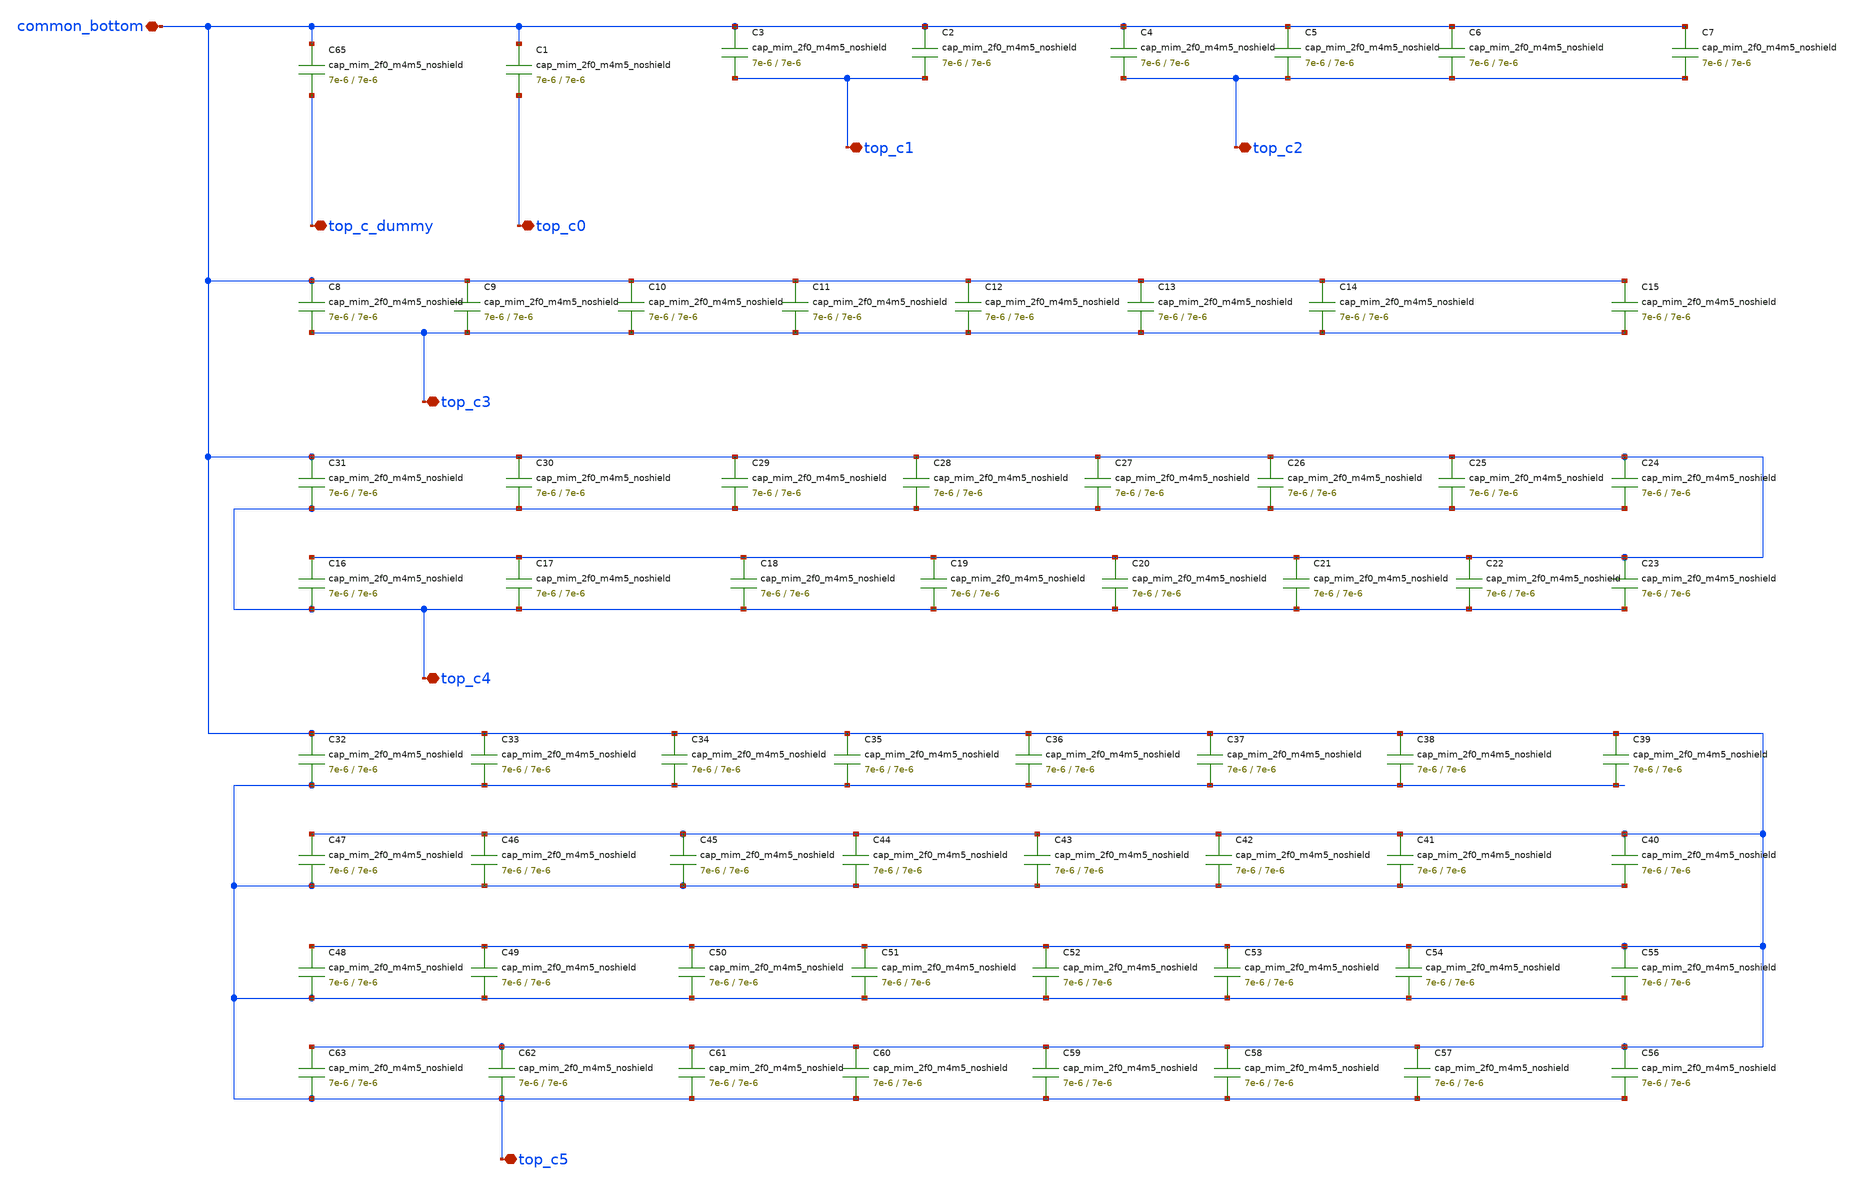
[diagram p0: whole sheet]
** sch_path: cdac/mim_cap_array_8x8/rev001/advanced_mimcap_array8x8_15step.sch
**.subckt advanced_mimcap_array8x8_15step common_bottom top_c1 top_c0 top_c_dummy top_c2 top_c4
*+ top_c5 top_c3
*.iopin common_bottom
*.iopin top_c1
*.iopin top_c0
*.iopin top_c_dummy
*.iopin top_c2
*.iopin top_c4
*.iopin top_c5
*.iopin top_c3
C65 common_bottom top_c_dummy cap_mim_2f0_m4m5_noshield W=7e-6 L=7e-6
C1 common_bottom top_c0 cap_mim_2f0_m4m5_noshield W=7e-6 L=7e-6
C2 common_bottom top_c1 cap_mim_2f0_m4m5_noshield W=7e-6 L=7e-6
C3 common_bottom top_c1 cap_mim_2f0_m4m5_noshield W=7e-6 L=7e-6
C4 common_bottom top_c2 cap_mim_2f0_m4m5_noshield W=7e-6 L=7e-6
C5 common_bottom top_c2 cap_mim_2f0_m4m5_noshield W=7e-6 L=7e-6
C6 common_bottom top_c2 cap_mim_2f0_m4m5_noshield W=7e-6 L=7e-6
C7 common_bottom top_c2 cap_mim_2f0_m4m5_noshield W=7e-6 L=7e-6
C8 common_bottom top_c3 cap_mim_2f0_m4m5_noshield W=7e-6 L=7e-6
C9 common_bottom top_c3 cap_mim_2f0_m4m5_noshield W=7e-6 L=7e-6
C10 common_bottom top_c3 cap_mim_2f0_m4m5_noshield W=7e-6 L=7e-6
C11 common_bottom top_c3 cap_mim_2f0_m4m5_noshield W=7e-6 L=7e-6
C12 common_bottom top_c3 cap_mim_2f0_m4m5_noshield W=7e-6 L=7e-6
C13 common_bottom top_c3 cap_mim_2f0_m4m5_noshield W=7e-6 L=7e-6
C14 common_bottom top_c3 cap_mim_2f0_m4m5_noshield W=7e-6 L=7e-6
C15 common_bottom top_c3 cap_mim_2f0_m4m5_noshield W=7e-6 L=7e-6
C16 common_bottom top_c4 cap_mim_2f0_m4m5_noshield W=7e-6 L=7e-6
C17 common_bottom top_c4 cap_mim_2f0_m4m5_noshield W=7e-6 L=7e-6
C18 common_bottom top_c4 cap_mim_2f0_m4m5_noshield W=7e-6 L=7e-6
C19 common_bottom top_c4 cap_mim_2f0_m4m5_noshield W=7e-6 L=7e-6
C20 common_bottom top_c4 cap_mim_2f0_m4m5_noshield W=7e-6 L=7e-6
C21 common_bottom top_c4 cap_mim_2f0_m4m5_noshield W=7e-6 L=7e-6
C22 common_bottom top_c4 cap_mim_2f0_m4m5_noshield W=7e-6 L=7e-6
C23 common_bottom top_c4 cap_mim_2f0_m4m5_noshield W=7e-6 L=7e-6
C24 common_bottom top_c4 cap_mim_2f0_m4m5_noshield W=7e-6 L=7e-6
C25 common_bottom top_c4 cap_mim_2f0_m4m5_noshield W=7e-6 L=7e-6
C26 common_bottom top_c4 cap_mim_2f0_m4m5_noshield W=7e-6 L=7e-6
C27 common_bottom top_c4 cap_mim_2f0_m4m5_noshield W=7e-6 L=7e-6
C28 common_bottom top_c4 cap_mim_2f0_m4m5_noshield W=7e-6 L=7e-6
C29 common_bottom top_c4 cap_mim_2f0_m4m5_noshield W=7e-6 L=7e-6
C30 common_bottom top_c4 cap_mim_2f0_m4m5_noshield W=7e-6 L=7e-6
C31 common_bottom top_c4 cap_mim_2f0_m4m5_noshield W=7e-6 L=7e-6
C32 common_bottom top_c5 cap_mim_2f0_m4m5_noshield W=7e-6 L=7e-6
C33 common_bottom top_c5 cap_mim_2f0_m4m5_noshield W=7e-6 L=7e-6
C34 common_bottom top_c5 cap_mim_2f0_m4m5_noshield W=7e-6 L=7e-6
C35 common_bottom top_c5 cap_mim_2f0_m4m5_noshield W=7e-6 L=7e-6
C36 common_bottom top_c5 cap_mim_2f0_m4m5_noshield W=7e-6 L=7e-6
C37 common_bottom top_c5 cap_mim_2f0_m4m5_noshield W=7e-6 L=7e-6
C38 common_bottom top_c5 cap_mim_2f0_m4m5_noshield W=7e-6 L=7e-6
C39 common_bottom top_c5 cap_mim_2f0_m4m5_noshield W=7e-6 L=7e-6
C40 common_bottom top_c5 cap_mim_2f0_m4m5_noshield W=7e-6 L=7e-6
C41 common_bottom top_c5 cap_mim_2f0_m4m5_noshield W=7e-6 L=7e-6
C42 common_bottom top_c5 cap_mim_2f0_m4m5_noshield W=7e-6 L=7e-6
C43 common_bottom top_c5 cap_mim_2f0_m4m5_noshield W=7e-6 L=7e-6
C44 common_bottom top_c5 cap_mim_2f0_m4m5_noshield W=7e-6 L=7e-6
C45 common_bottom top_c5 cap_mim_2f0_m4m5_noshield W=7e-6 L=7e-6
C46 common_bottom top_c5 cap_mim_2f0_m4m5_noshield W=7e-6 L=7e-6
C47 common_bottom top_c5 cap_mim_2f0_m4m5_noshield W=7e-6 L=7e-6
C48 common_bottom top_c5 cap_mim_2f0_m4m5_noshield W=7e-6 L=7e-6
C49 common_bottom top_c5 cap_mim_2f0_m4m5_noshield W=7e-6 L=7e-6
C50 common_bottom top_c5 cap_mim_2f0_m4m5_noshield W=7e-6 L=7e-6
C51 common_bottom top_c5 cap_mim_2f0_m4m5_noshield W=7e-6 L=7e-6
C52 common_bottom top_c5 cap_mim_2f0_m4m5_noshield W=7e-6 L=7e-6
C53 common_bottom top_c5 cap_mim_2f0_m4m5_noshield W=7e-6 L=7e-6
C54 common_bottom top_c5 cap_mim_2f0_m4m5_noshield W=7e-6 L=7e-6
C55 common_bottom top_c5 cap_mim_2f0_m4m5_noshield W=7e-6 L=7e-6
C56 common_bottom top_c5 cap_mim_2f0_m4m5_noshield W=7e-6 L=7e-6
C57 common_bottom top_c5 cap_mim_2f0_m4m5_noshield W=7e-6 L=7e-6
C58 common_bottom top_c5 cap_mim_2f0_m4m5_noshield W=7e-6 L=7e-6
C59 common_bottom top_c5 cap_mim_2f0_m4m5_noshield W=7e-6 L=7e-6
C60 common_bottom top_c5 cap_mim_2f0_m4m5_noshield W=7e-6 L=7e-6
C61 common_bottom top_c5 cap_mim_2f0_m4m5_noshield W=7e-6 L=7e-6
C62 common_bottom top_c5 cap_mim_2f0_m4m5_noshield W=7e-6 L=7e-6
C63 common_bottom top_c5 cap_mim_2f0_m4m5_noshield W=7e-6 L=7e-6
**.ends
.end
